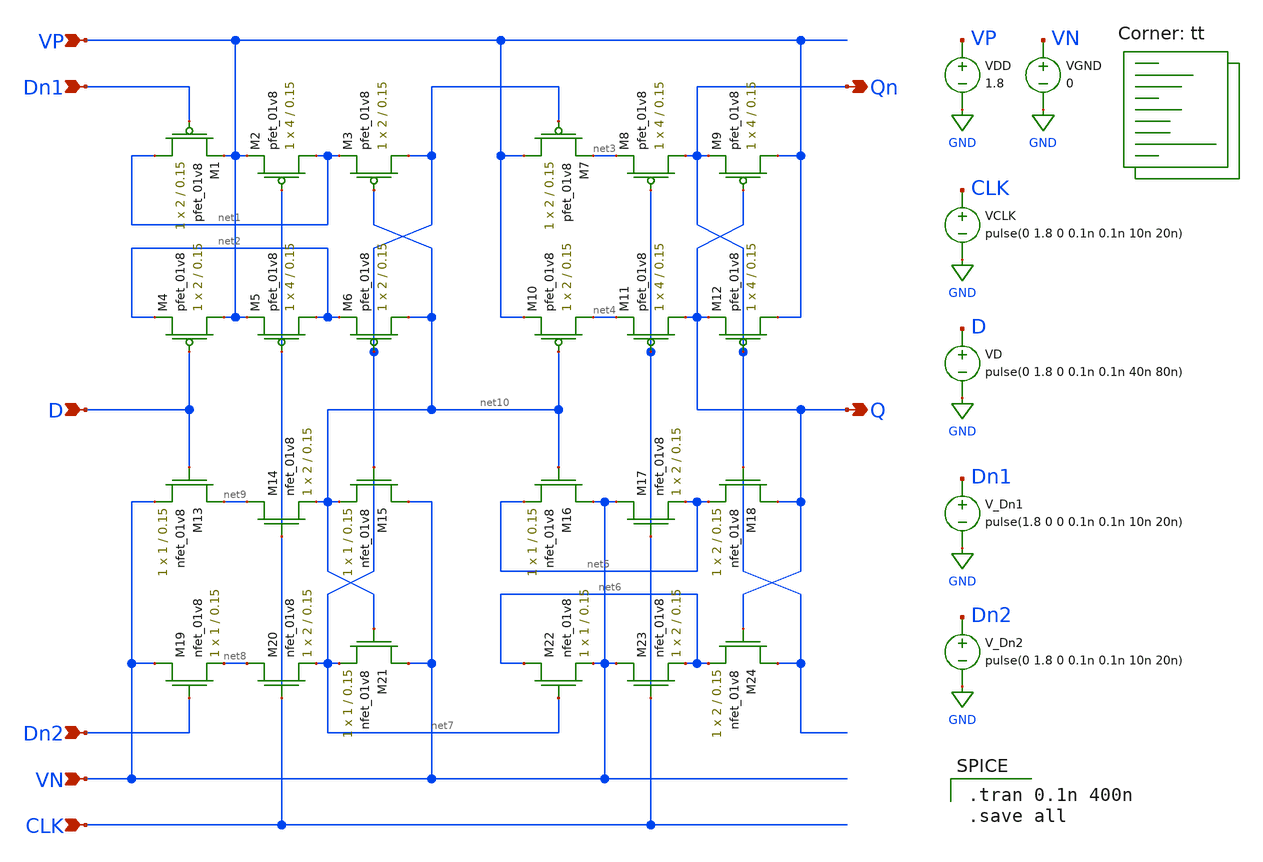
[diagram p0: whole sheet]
** sch_path: Mixed-Signal TRNG/xschem/dff.sch
**.subckt dff Qn Q Dn1 D Dn2 CLK VP VN
*.opin Qn
*.opin Q
*.ipin Dn1
*.ipin D
*.ipin Dn2
*.ipin CLK
*.ipin VP
*.ipin VN
XM1 net1 Dn1 VP VP sky130_fd_pr__pfet_01v8 L=0.15 W=2 nf=1 ad='int((nf+1)/2) * W/nf * 0.29' as='int((nf+2)/2) * W/nf * 0.29'
+ pd='2*int((nf+1)/2) * (W/nf + 0.29)' ps='2*int((nf+2)/2) * (W/nf + 0.29)' nrd='0.29 / W' nrs='0.29 / W'
+ sa=0 sb=0 sd=0 mult=1 m=1
XM2 net1 CLK VP VP sky130_fd_pr__pfet_01v8 L=0.15 W=4 nf=1 ad='int((nf+1)/2) * W/nf * 0.29' as='int((nf+2)/2) * W/nf * 0.29'
+ pd='2*int((nf+1)/2) * (W/nf + 0.29)' ps='2*int((nf+2)/2) * (W/nf + 0.29)' nrd='0.29 / W' nrs='0.29 / W'
+ sa=0 sb=0 sd=0 mult=1 m=1
XM3 net7 net10 net1 VP sky130_fd_pr__pfet_01v8 L=0.15 W=2 nf=1 ad='int((nf+1)/2) * W/nf * 0.29' as='int((nf+2)/2) * W/nf * 0.29'
+ pd='2*int((nf+1)/2) * (W/nf + 0.29)' ps='2*int((nf+2)/2) * (W/nf + 0.29)' nrd='0.29 / W' nrs='0.29 / W'
+ sa=0 sb=0 sd=0 mult=1 m=1
XM4 VP D net2 VP sky130_fd_pr__pfet_01v8 L=0.15 W=2 nf=1 ad='int((nf+1)/2) * W/nf * 0.29' as='int((nf+2)/2) * W/nf * 0.29'
+ pd='2*int((nf+1)/2) * (W/nf + 0.29)' ps='2*int((nf+2)/2) * (W/nf + 0.29)' nrd='0.29 / W' nrs='0.29 / W'
+ sa=0 sb=0 sd=0 mult=1 m=1
XM5 net2 CLK VP VP sky130_fd_pr__pfet_01v8 L=0.15 W=4 nf=1 ad='int((nf+1)/2) * W/nf * 0.29' as='int((nf+2)/2) * W/nf * 0.29'
+ pd='2*int((nf+1)/2) * (W/nf + 0.29)' ps='2*int((nf+2)/2) * (W/nf + 0.29)' nrd='0.29 / W' nrs='0.29 / W'
+ sa=0 sb=0 sd=0 mult=1 m=1
XM6 net10 net7 net2 VP sky130_fd_pr__pfet_01v8 L=0.15 W=2 nf=1 ad='int((nf+1)/2) * W/nf * 0.29' as='int((nf+2)/2) * W/nf * 0.29'
+ pd='2*int((nf+1)/2) * (W/nf + 0.29)' ps='2*int((nf+2)/2) * (W/nf + 0.29)' nrd='0.29 / W' nrs='0.29 / W'
+ sa=0 sb=0 sd=0 mult=1 m=1
XM7 VP net7 net3 VP sky130_fd_pr__pfet_01v8 L=0.15 W=2 nf=1 ad='int((nf+1)/2) * W/nf * 0.29' as='int((nf+2)/2) * W/nf * 0.29'
+ pd='2*int((nf+1)/2) * (W/nf + 0.29)' ps='2*int((nf+2)/2) * (W/nf + 0.29)' nrd='0.29 / W' nrs='0.29 / W'
+ sa=0 sb=0 sd=0 mult=1 m=1
XM8 Qn CLK net3 VP sky130_fd_pr__pfet_01v8 L=0.15 W=4 nf=1 ad='int((nf+1)/2) * W/nf * 0.29' as='int((nf+2)/2) * W/nf * 0.29'
+ pd='2*int((nf+1)/2) * (W/nf + 0.29)' ps='2*int((nf+2)/2) * (W/nf + 0.29)' nrd='0.29 / W' nrs='0.29 / W'
+ sa=0 sb=0 sd=0 mult=1 m=1
XM9 VP Q Qn VP sky130_fd_pr__pfet_01v8 L=0.15 W=4 nf=1 ad='int((nf+1)/2) * W/nf * 0.29' as='int((nf+2)/2) * W/nf * 0.29'
+ pd='2*int((nf+1)/2) * (W/nf + 0.29)' ps='2*int((nf+2)/2) * (W/nf + 0.29)' nrd='0.29 / W' nrs='0.29 / W'
+ sa=0 sb=0 sd=0 mult=1 m=1
XM10 net4 net10 VP VP sky130_fd_pr__pfet_01v8 L=0.15 W=2 nf=1 ad='int((nf+1)/2) * W/nf * 0.29' as='int((nf+2)/2) * W/nf * 0.29'
+ pd='2*int((nf+1)/2) * (W/nf + 0.29)' ps='2*int((nf+2)/2) * (W/nf + 0.29)' nrd='0.29 / W' nrs='0.29 / W'
+ sa=0 sb=0 sd=0 mult=1 m=1
XM11 Q CLK net4 VP sky130_fd_pr__pfet_01v8 L=0.15 W=4 nf=1 ad='int((nf+1)/2) * W/nf * 0.29' as='int((nf+2)/2) * W/nf * 0.29'
+ pd='2*int((nf+1)/2) * (W/nf + 0.29)' ps='2*int((nf+2)/2) * (W/nf + 0.29)' nrd='0.29 / W' nrs='0.29 / W'
+ sa=0 sb=0 sd=0 mult=1 m=1
XM12 VP Qn Q VP sky130_fd_pr__pfet_01v8 L=0.15 W=4 nf=1 ad='int((nf+1)/2) * W/nf * 0.29' as='int((nf+2)/2) * W/nf * 0.29'
+ pd='2*int((nf+1)/2) * (W/nf + 0.29)' ps='2*int((nf+2)/2) * (W/nf + 0.29)' nrd='0.29 / W' nrs='0.29 / W'
+ sa=0 sb=0 sd=0 mult=1 m=1
XM13 net9 D VN VN sky130_fd_pr__nfet_01v8 L=0.15 W=1 nf=1 ad='int((nf+1)/2) * W/nf * 0.29' as='int((nf+2)/2) * W/nf * 0.29'
+ pd='2*int((nf+1)/2) * (W/nf + 0.29)' ps='2*int((nf+2)/2) * (W/nf + 0.29)' nrd='0.29 / W' nrs='0.29 / W'
+ sa=0 sb=0 sd=0 mult=1 m=1
XM14 net9 CLK net10 VN sky130_fd_pr__nfet_01v8 L=0.15 W=2 nf=1 ad='int((nf+1)/2) * W/nf * 0.29' as='int((nf+2)/2) * W/nf * 0.29'
+ pd='2*int((nf+1)/2) * (W/nf + 0.29)' ps='2*int((nf+2)/2) * (W/nf + 0.29)' nrd='0.29 / W' nrs='0.29 / W'
+ sa=0 sb=0 sd=0 mult=1 m=1
XM15 VN net7 net10 VN sky130_fd_pr__nfet_01v8 L=0.15 W=1 nf=1 ad='int((nf+1)/2) * W/nf * 0.29' as='int((nf+2)/2) * W/nf * 0.29'
+ pd='2*int((nf+1)/2) * (W/nf + 0.29)' ps='2*int((nf+2)/2) * (W/nf + 0.29)' nrd='0.29 / W' nrs='0.29 / W'
+ sa=0 sb=0 sd=0 mult=1 m=1
XM16 VN net10 net5 VN sky130_fd_pr__nfet_01v8 L=0.15 W=1 nf=1 ad='int((nf+1)/2) * W/nf * 0.29' as='int((nf+2)/2) * W/nf * 0.29'
+ pd='2*int((nf+1)/2) * (W/nf + 0.29)' ps='2*int((nf+2)/2) * (W/nf + 0.29)' nrd='0.29 / W' nrs='0.29 / W'
+ sa=0 sb=0 sd=0 mult=1 m=1
XM17 VN CLK net5 VN sky130_fd_pr__nfet_01v8 L=0.15 W=2 nf=1 ad='int((nf+1)/2) * W/nf * 0.29' as='int((nf+2)/2) * W/nf * 0.29'
+ pd='2*int((nf+1)/2) * (W/nf + 0.29)' ps='2*int((nf+2)/2) * (W/nf + 0.29)' nrd='0.29 / W' nrs='0.29 / W'
+ sa=0 sb=0 sd=0 mult=1 m=1
XM18 Q Qn net5 VN sky130_fd_pr__nfet_01v8 L=0.15 W=2 nf=1 ad='int((nf+1)/2) * W/nf * 0.29' as='int((nf+2)/2) * W/nf * 0.29'
+ pd='2*int((nf+1)/2) * (W/nf + 0.29)' ps='2*int((nf+2)/2) * (W/nf + 0.29)' nrd='0.29 / W' nrs='0.29 / W'
+ sa=0 sb=0 sd=0 mult=1 m=1
XM19 VN Dn2 net8 VN sky130_fd_pr__nfet_01v8 L=0.15 W=1 nf=1 ad='int((nf+1)/2) * W/nf * 0.29' as='int((nf+2)/2) * W/nf * 0.29'
+ pd='2*int((nf+1)/2) * (W/nf + 0.29)' ps='2*int((nf+2)/2) * (W/nf + 0.29)' nrd='0.29 / W' nrs='0.29 / W'
+ sa=0 sb=0 sd=0 mult=1 m=1
XM20 net8 CLK net7 VN sky130_fd_pr__nfet_01v8 L=0.15 W=2 nf=1 ad='int((nf+1)/2) * W/nf * 0.29' as='int((nf+2)/2) * W/nf * 0.29'
+ pd='2*int((nf+1)/2) * (W/nf + 0.29)' ps='2*int((nf+2)/2) * (W/nf + 0.29)' nrd='0.29 / W' nrs='0.29 / W'
+ sa=0 sb=0 sd=0 mult=1 m=1
XM21 VN net10 net7 VN sky130_fd_pr__nfet_01v8 L=0.15 W=1 nf=1 ad='int((nf+1)/2) * W/nf * 0.29' as='int((nf+2)/2) * W/nf * 0.29'
+ pd='2*int((nf+1)/2) * (W/nf + 0.29)' ps='2*int((nf+2)/2) * (W/nf + 0.29)' nrd='0.29 / W' nrs='0.29 / W'
+ sa=0 sb=0 sd=0 mult=1 m=1
XM22 net6 net7 VN VN sky130_fd_pr__nfet_01v8 L=0.15 W=1 nf=1 ad='int((nf+1)/2) * W/nf * 0.29' as='int((nf+2)/2) * W/nf * 0.29'
+ pd='2*int((nf+1)/2) * (W/nf + 0.29)' ps='2*int((nf+2)/2) * (W/nf + 0.29)' nrd='0.29 / W' nrs='0.29 / W'
+ sa=0 sb=0 sd=0 mult=1 m=1
XM23 VN CLK net6 VN sky130_fd_pr__nfet_01v8 L=0.15 W=2 nf=1 ad='int((nf+1)/2) * W/nf * 0.29' as='int((nf+2)/2) * W/nf * 0.29'
+ pd='2*int((nf+1)/2) * (W/nf + 0.29)' ps='2*int((nf+2)/2) * (W/nf + 0.29)' nrd='0.29 / W' nrs='0.29 / W'
+ sa=0 sb=0 sd=0 mult=1 m=1
XM24 Qn Q net6 VN sky130_fd_pr__nfet_01v8 L=0.15 W=2 nf=1 ad='int((nf+1)/2) * W/nf * 0.29' as='int((nf+2)/2) * W/nf * 0.29'
+ pd='2*int((nf+1)/2) * (W/nf + 0.29)' ps='2*int((nf+2)/2) * (W/nf + 0.29)' nrd='0.29 / W' nrs='0.29 / W'
+ sa=0 sb=0 sd=0 mult=1 m=1
VDD VP GND 1.8
VGND VN GND 0
VCLK CLK GND pulse(0 1.8 0 0.1n 0.1n 10n 20n)
VD D GND pulse(0 1.8 0 0.1n 0.1n 40n 80n)
V_Dn1 Dn1 GND pulse(1.8 0 0 0.1n 0.1n 10n 20n)
V_Dn2 Dn2 GND pulse(0 1.8 0 0.1n 0.1n 10n 20n)
**** begin user architecture code
.lib $::SKYWATER_MODELS/sky130.lib.spice tt

.tran 0.1n 400n
.save all

**** end user architecture code
**.ends
.GLOBAL GND
.end
